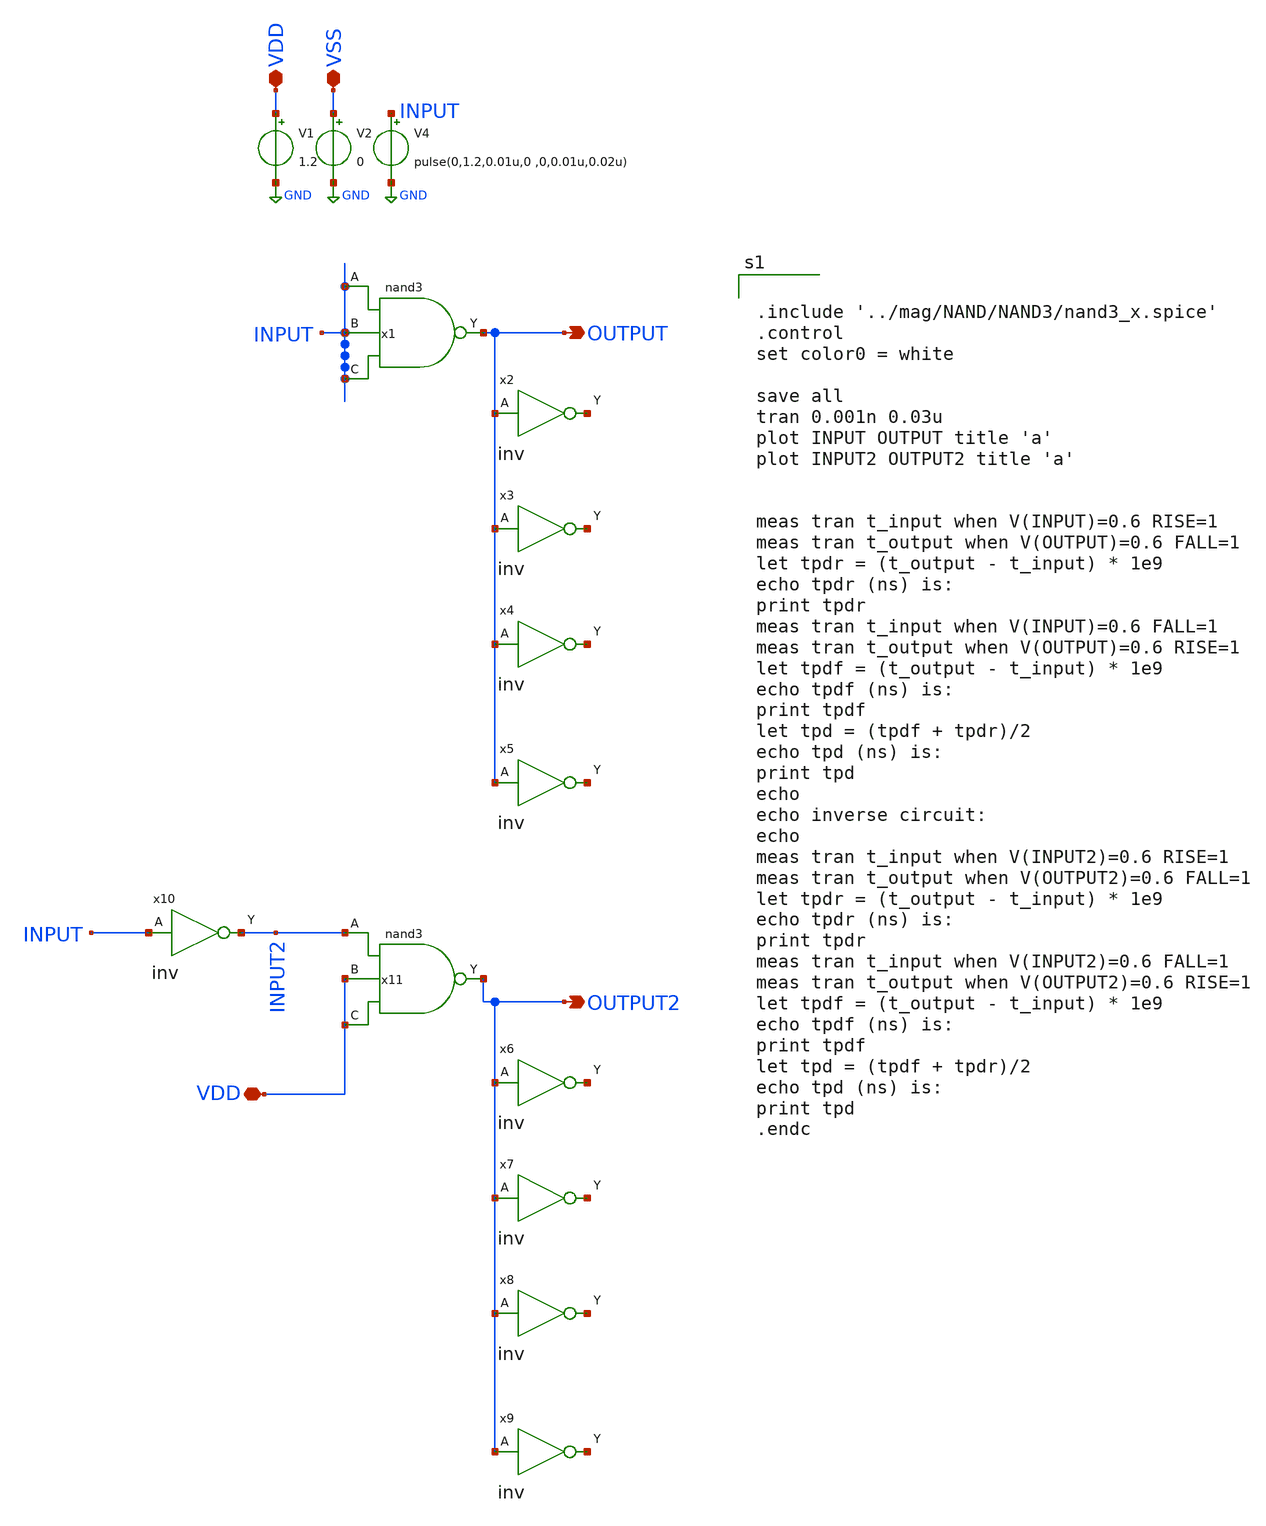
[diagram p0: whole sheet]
** sch_path: design/xschem/From Layout/NAND/nand3_TB.sch
**.subckt nand3_TB OUTPUT VDD VSS OUTPUT2 VDD
*.opin OUTPUT
*.iopin VDD
*.iopin VSS
*.opin OUTPUT2
*.iopin VDD
V1 VDD GND 1.2
V2 VSS GND 0
V4 INPUT GND pulse(0,1.2,0.01u,0 ,0,0.01u,0.02u)
x2 OUTPUT VSS VDD net1 inv
x3 OUTPUT VSS VDD net2 inv
x4 OUTPUT VSS VDD net3 inv
x5 OUTPUT VSS VDD net4 inv
x6 OUTPUT2 VSS VDD net5 inv
x7 OUTPUT2 VSS VDD net6 inv
x8 OUTPUT2 VSS VDD net7 inv
x9 OUTPUT2 VSS VDD net8 inv
x10 INPUT VSS VDD INPUT2 inv
x1 INPUT INPUT INPUT VSS VDD OUTPUT nand3
x11 INPUT2 VDD VDD VSS VDD OUTPUT2 nand3
**** begin user architecture code

** opencircuitdesign pdks install
.lib $::SKYWATER_MODELS/sky130.lib.spice tt_mm




.include '../mag/NAND/NAND3/nand3_x.spice'
.control
set color0 = white

save all
tran 0.001n 0.03u
plot INPUT OUTPUT title 'a'
plot INPUT2 OUTPUT2 title 'a'


meas tran t_input when V(INPUT)=0.6 RISE=1
meas tran t_output when V(OUTPUT)=0.6 FALL=1
let tpdr = (t_output - t_input) * 1e9
echo tpdr (ns) is:
print tpdr
meas tran t_input when V(INPUT)=0.6 FALL=1
meas tran t_output when V(OUTPUT)=0.6 RISE=1
let tpdf = (t_output - t_input) * 1e9
echo tpdf (ns) is:
print tpdf
let tpd = (tpdf + tpdr)/2
echo tpd (ns) is:
print tpd
echo
echo inverse circuit:
echo
meas tran t_input when V(INPUT2)=0.6 RISE=1
meas tran t_output when V(OUTPUT2)=0.6 FALL=1
let tpdr = (t_output - t_input) * 1e9
echo tpdr (ns) is:
print tpdr
meas tran t_input when V(INPUT2)=0.6 FALL=1
meas tran t_output when V(OUTPUT2)=0.6 RISE=1
let tpdf = (t_output - t_input) * 1e9
echo tpdf (ns) is:
print tpdf
let tpd = (tpdf + tpdr)/2
echo tpd (ns) is:
print tpd
.endc


**** end user architecture code
**.ends
.GLOBAL GND
.end
